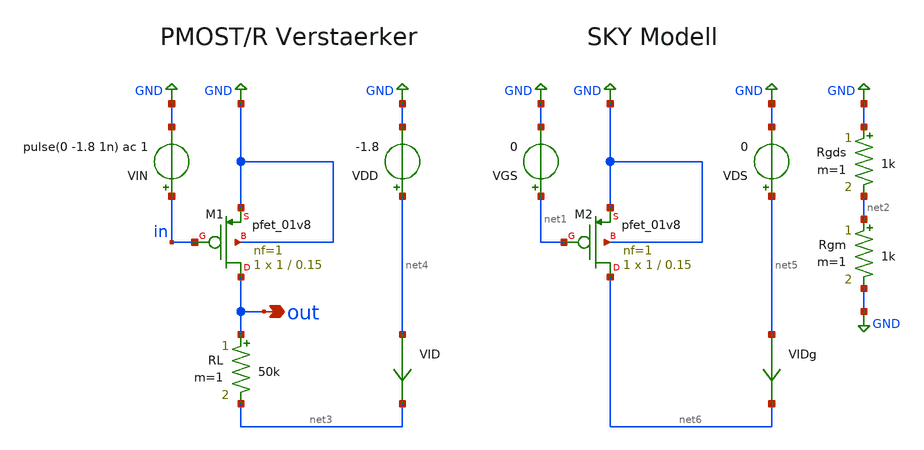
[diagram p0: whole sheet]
** sch_path: Abgaben/Aufgabe1_k12136610.sch
**.subckt Aufgabe1_k12136610 out
*.opin out
XM1 out in GND GND sky130_fd_pr__pfet_01v8 L=0.15 W=1 nf=1 ad='int((1 + 1)/2) * 1 / 1 * 0.29' as='int((1 + 2)/2) * 1 / 1 * 0.29'
+ pd='2*int((1 + 1)/2) * (1 / 1 + 0.29)' ps='2*int((1 + 2)/2) * (1 / 1 + 0.29)' nrd='0.29 / 1 ' nrs='0.29 / 1 '
+ sa=0 sb=0 sd=0 mult=1 m=1
VIN in GND pulse(0 -1.8 1n) ac 1
VDD net4 GND -1.8
RL out net3 50k m=1
XM2 net6 net1 GND GND sky130_fd_pr__pfet_01v8 L=0.15 W=1 nf=1 ad='int((1 + 1)/2) * 1 / 1 * 0.29' as='int((1 + 2)/2) * 1 / 1 * 0.29'
+ pd='2*int((1 + 1)/2) * (1 / 1 + 0.29)' ps='2*int((1 + 2)/2) * (1 / 1 + 0.29)' nrd='0.29 / 1 ' nrs='0.29 / 1 '
+ sa=0 sb=0 sd=0 mult=1 m=1
VGS net1 GND 0
VDS net5 GND 0
Rgds GND net2 1k m=1
Rgm net2 GND 1k m=1
VIDg net5 net6 0
.save i(vidg)
VID net4 net3 0
.save i(vid)
**** begin user architecture code


.lib /foss/pdks/sky130A/libs.tech/ngspice/sky130.lib.spice tt

.control
set xbrushwidth=7
set xgridwidth=2
set xfont_size=20

alter @RL[resistance]=50k

*******************
*** DC Analysis ***
*******************

dc VIN 0 -1.8 -1m
let A0=deriv(-out)
plot out
plot A0

***********************
*** Operating Point ***
***********************

meas DC A0max max A0
meas DC vgs_op max_at A0
meas DC vds_op find out at=vgs_op

alter @VGS[dc]=vgs_op
alter @VDS[dc]=vds_op

dc VDS 0 -1.8 -1m
let func_gds=deriv(I(VIDg))
plot func_gds
meas DC gds find func_gds at=@VDS[dc]
alter @Rgds[resistance]=1/gds

dc VGS 0 -1.8 -1m
let func_gm=deriv(I(VIDg))
plot func_gm
meas DC gm find func_gm at=@VGS[dc]
alter @Rgm[resistance]=1/gm

let A0_calc=1/(@Rgm[resistance]*(1/@Rgds[resistance]+1/@RL[resistance]))
print A0_calc

.endc
.save all




.control
set xbrushwidth=7
set xgridwidth=2
set xfont_size=20

**************************
*** Transient Analysis ***
**************************

tran 25p 3n
plot in out

.endc
.save all




.control
set xbrushwidth=7
set xgridwidth=2
set xfont_size=20

**************************
*** AC Analysis ***
**************************

alter @VIN[ac]=-1.8
ac dec 100 1 100G
plot -v(out)/v(in)
plot phase(-v(out)/v(in))

.endc
.save all


**** end user architecture code
**.ends
.GLOBAL GND
.end
